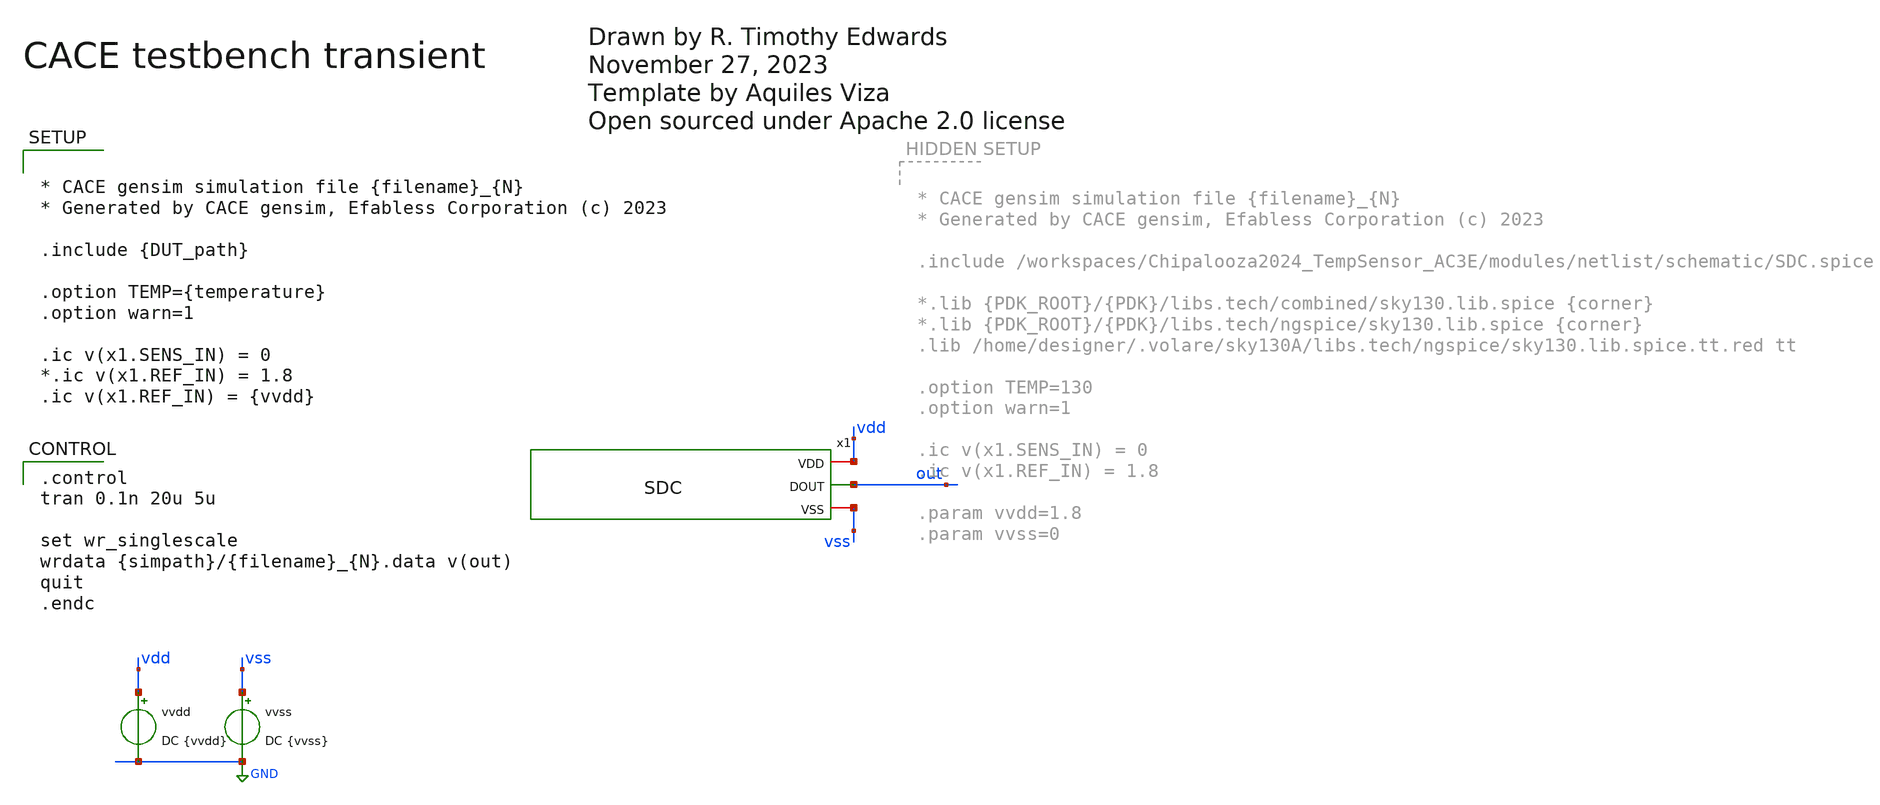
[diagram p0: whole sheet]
** sch_path: modules/SDC/cace/transient.sch
* Open sourced under Apache 2.0 license


* CACE gensim simulation file {filename}_{N}
* Generated by CACE gensim, Efabless Corporation (c) 2023

.include {DUT_path}

.option TEMP={temperature}
.option warn=1

.ic v(x1.SENS_IN) = 0
*.ic v(x1.REF_IN) = 1.8
.ic v(x1.REF_IN) = {vvdd}


**.subckt transient
vvss vss GND DC {vvss}
vvdd vdd GND DC {vvdd}
x1 vdd out vss SDC
**** begin user architecture code

.control
tran 0.1n 20u 5u

set wr_singlescale
wrdata {simpath}/{filename}_{N}.data v(out)
quit
.endc



*.lib $env(PDK_ROOT)/$env(PDK)/libs.tech/ngspice/sky130.lib.spice.{corner}.red {corner}
.lib $env(PDK_ROOT)/$env(PDK)/libs.tech/combined/sky130.lib.spice {corner}

.include $env(PDK_ROOT)/$env(PDK)/libs.ref/sky130_fd_sc_hd/spice/sky130_fd_sc_hd.spice

**** end user architecture code
**.ends
.GLOBAL GND
.end
